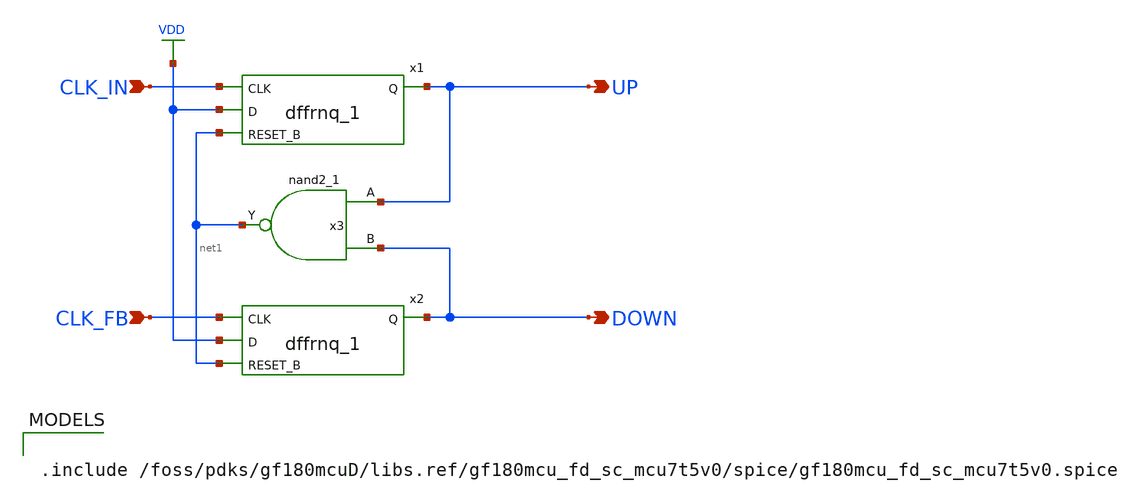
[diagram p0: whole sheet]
** sch_path: designs/libs/core_analog/pfd/pfd.sch
**.subckt pfd UP DOWN CLK_IN CLK_FB
*.opin UP
*.opin DOWN
*.ipin CLK_IN
*.ipin CLK_FB
x1 VDD net1 CLK_IN UP VDD VDD VSS VSS gf180mcu_fd_sc_mcu7t5v0__dffrnq_1
x2 VDD net1 CLK_FB DOWN VDD VDD VSS VSS gf180mcu_fd_sc_mcu7t5v0__dffrnq_1
x3 UP DOWN net1 VDD VDD VSS VSS gf180mcu_fd_sc_mcu7t5v0__nand2_1
**** begin user architecture code

.include /foss/pdks/gf180mcuD/libs.ref/gf180mcu_fd_sc_mcu7t5v0/spice/gf180mcu_fd_sc_mcu7t5v0.spice


**** end user architecture code
**.ends
.GLOBAL VDD
.end
